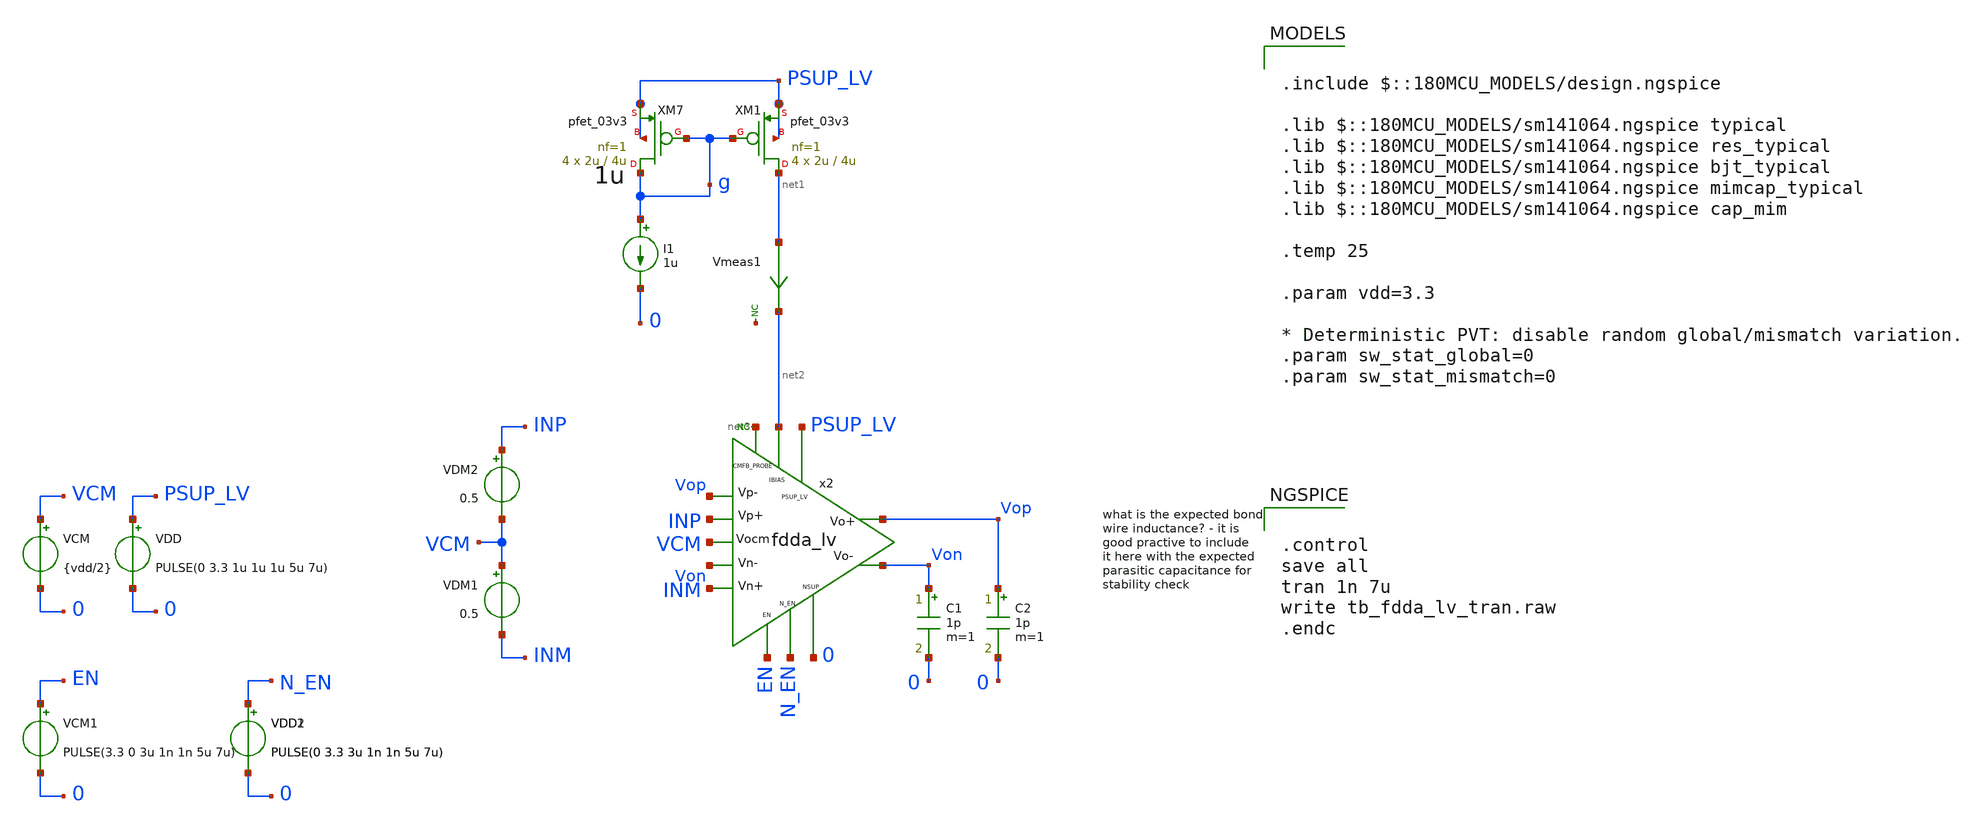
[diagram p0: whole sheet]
** sch_path: xschem/blocks/fdda_lv/tb_fdda_lv_tran.sch
**.subckt tb_fdda_lv_tran
C1 Von 0 1p m=1
x2 PSUP_LV Vop Von INM INP Vop Von net2 N_EN EN 0 net3 VCM fdda_lv
VDD PSUP_LV 0 PULSE(0 3.3 1u 1u 1u 5u 7u)
C2 Vop 0 1p m=1
VCM VCM 0 {vdd/2}
VDM2 INP VCM 0.5
VDM1 VCM INM 0.5
* noconn #net3
* noconn #net4
XM7 g g PSUP_LV PSUP_LV pfet_03v3 L=4u W=2u nf=1 ad='int((nf+1)/2) * W/nf * 0.18u' as='int((nf+2)/2) * W/nf * 0.18u'
+ pd='2*int((nf+1)/2) * (W/nf + 0.18u)' ps='2*int((nf+2)/2) * (W/nf + 0.18u)' nrd='0.18u / W' nrs='0.18u / W'
+ sa=0 sb=0 sd=0 m=4
XM1 net1 g PSUP_LV PSUP_LV pfet_03v3 L=4u W=2u nf=1 ad='int((nf+1)/2) * W/nf * 0.18u' as='int((nf+2)/2) * W/nf * 0.18u'
+ pd='2*int((nf+1)/2) * (W/nf + 0.18u)' ps='2*int((nf+2)/2) * (W/nf + 0.18u)' nrd='0.18u / W' nrs='0.18u / W'
+ sa=0 sb=0 sd=0 m=4
I1 g 0 1u
Vmeas1 net1 net2 0
.save i(vmeas1)
VDD1 N_EN 0 PULSE(0 3.3 3u 1n 1n 5u 7u)
VCM1 EN 0 PULSE(3.3 0 3u 1n 1n 5u 7u)
VDD2 N_EN 0 PULSE(0 3.3 3u 1n 1n 5u 7u)
**** begin user architecture code

.include $::180MCU_MODELS/design.ngspice

.lib $::180MCU_MODELS/sm141064.ngspice typical
.lib $::180MCU_MODELS/sm141064.ngspice res_typical
.lib $::180MCU_MODELS/sm141064.ngspice bjt_typical
.lib $::180MCU_MODELS/sm141064.ngspice mimcap_typical
.lib $::180MCU_MODELS/sm141064.ngspice cap_mim

.temp 25

.param vdd=3.3

* Deterministic PVT: disable random global/mismatch variation.
.param sw_stat_global=0
.param sw_stat_mismatch=0



.control
save all
tran 1n 7u
write tb_fdda_lv_tran.raw
.endc


**** end user architecture code
**.ends
.end
